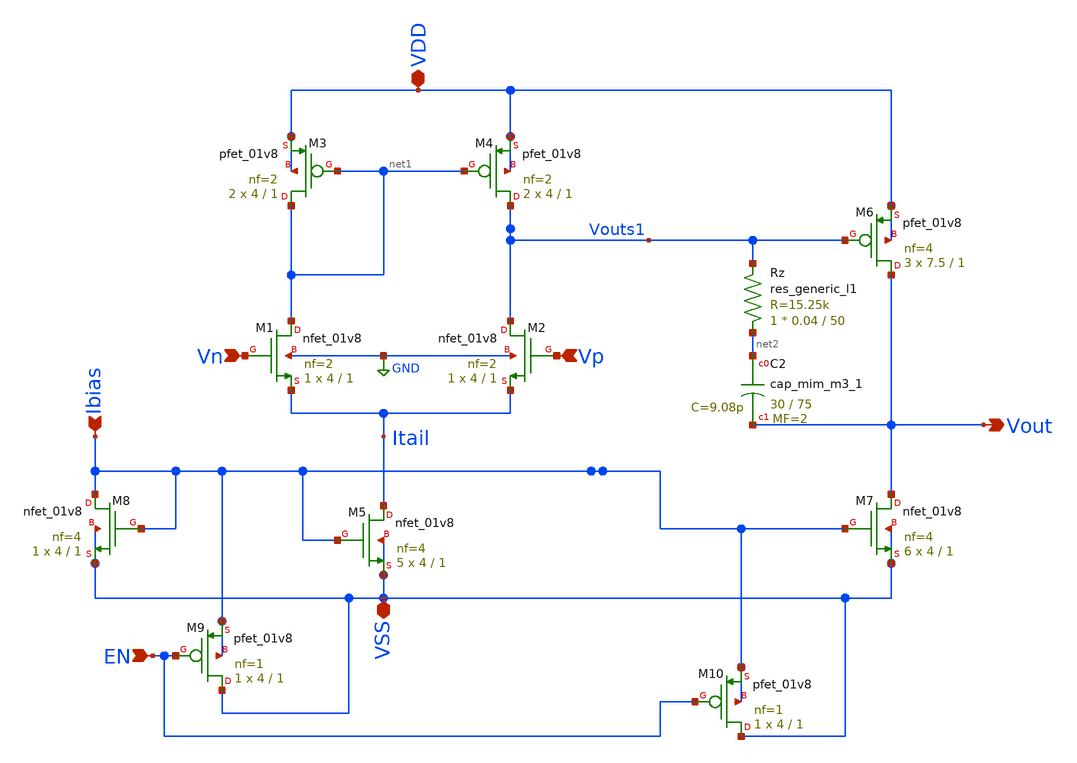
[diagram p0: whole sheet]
** sch_path: xschem/Opamp.sch
**.subckt Opamp Vn Ibias Vp EN Vout VSS VDD
*.ipin Vn
*.ipin Ibias
*.ipin Vp
*.ipin EN
*.opin Vout
*.iopin VSS
*.iopin VDD
XM2 Vouts1 Vp Itail GND sky130_fd_pr__nfet_01v8 L=1 W=4 nf=2 ad='int((nf+1)/2) * W/nf * 0.29' as='int((nf+2)/2) * W/nf * 0.29'
+ pd='2*int((nf+1)/2) * (W/nf + 0.29)' ps='2*int((nf+2)/2) * (W/nf + 0.29)' nrd='0.29 / W' nrs='0.29 / W'
+ sa=0 sb=0 sd=0 mult=1 m=1
XM4 Vouts1 net1 VDD VDD sky130_fd_pr__pfet_01v8 L=1 W=4 nf=2 ad='int((nf+1)/2) * W/nf * 0.29' as='int((nf+2)/2) * W/nf * 0.29'
+ pd='2*int((nf+1)/2) * (W/nf + 0.29)' ps='2*int((nf+2)/2) * (W/nf + 0.29)' nrd='0.29 / W' nrs='0.29 / W'
+ sa=0 sb=0 sd=0 mult=2 m=2
XM3 net1 net1 VDD VDD sky130_fd_pr__pfet_01v8 L=1 W=4 nf=2 ad='int((nf+1)/2) * W/nf * 0.29' as='int((nf+2)/2) * W/nf * 0.29'
+ pd='2*int((nf+1)/2) * (W/nf + 0.29)' ps='2*int((nf+2)/2) * (W/nf + 0.29)' nrd='0.29 / W' nrs='0.29 / W'
+ sa=0 sb=0 sd=0 mult=2 m=2
XM1 net1 Vn Itail GND sky130_fd_pr__nfet_01v8 L=1 W=4 nf=2 ad='int((nf+1)/2) * W/nf * 0.29' as='int((nf+2)/2) * W/nf * 0.29'
+ pd='2*int((nf+1)/2) * (W/nf + 0.29)' ps='2*int((nf+2)/2) * (W/nf + 0.29)' nrd='0.29 / W' nrs='0.29 / W'
+ sa=0 sb=0 sd=0 mult=1 m=1
XM6 Vout Vouts1 VDD VDD sky130_fd_pr__pfet_01v8 L=1 W=7.5 nf=4 ad='int((nf+1)/2) * W/nf * 0.29' as='int((nf+2)/2) * W/nf * 0.29'
+ pd='2*int((nf+1)/2) * (W/nf + 0.29)' ps='2*int((nf+2)/2) * (W/nf + 0.29)' nrd='0.29 / W' nrs='0.29 / W'
+ sa=0 sb=0 sd=0 mult=3 m=3
XM5 Itail Ibias VSS VSS sky130_fd_pr__nfet_01v8 L=1 W=4 nf=4 ad='int((nf+1)/2) * W/nf * 0.29' as='int((nf+2)/2) * W/nf * 0.29'
+ pd='2*int((nf+1)/2) * (W/nf + 0.29)' ps='2*int((nf+2)/2) * (W/nf + 0.29)' nrd='0.29 / W' nrs='0.29 / W'
+ sa=0 sb=0 sd=0 mult=5 m=5
XM7 Vout Ibias VSS VSS sky130_fd_pr__nfet_01v8 L=1 W=4 nf=4 ad='int((nf+1)/2) * W/nf * 0.29' as='int((nf+2)/2) * W/nf * 0.29'
+ pd='2*int((nf+1)/2) * (W/nf + 0.29)' ps='2*int((nf+2)/2) * (W/nf + 0.29)' nrd='0.29 / W' nrs='0.29 / W'
+ sa=0 sb=0 sd=0 mult=6 m=6
XM8 Ibias Ibias VSS VSS sky130_fd_pr__nfet_01v8 L=1 W=4 nf=4 ad='int((nf+1)/2) * W/nf * 0.29' as='int((nf+2)/2) * W/nf * 0.29'
+ pd='2*int((nf+1)/2) * (W/nf + 0.29)' ps='2*int((nf+2)/2) * (W/nf + 0.29)' nrd='0.29 / W' nrs='0.29 / W'
+ sa=0 sb=0 sd=0 mult=1 m=1
XM9 VSS EN Ibias Ibias sky130_fd_pr__pfet_01v8 L=1 W=4 nf=1 ad='int((nf+1)/2) * W/nf * 0.29' as='int((nf+2)/2) * W/nf * 0.29'
+ pd='2*int((nf+1)/2) * (W/nf + 0.29)' ps='2*int((nf+2)/2) * (W/nf + 0.29)' nrd='0.29 / W' nrs='0.29 / W'
+ sa=0 sb=0 sd=0 mult=1 m=1
XM10 VSS EN Ibias Ibias sky130_fd_pr__pfet_01v8 L=1 W=4 nf=1 ad='int((nf+1)/2) * W/nf * 0.29' as='int((nf+2)/2) * W/nf * 0.29'
+ pd='2*int((nf+1)/2) * (W/nf + 0.29)' ps='2*int((nf+2)/2) * (W/nf + 0.29)' nrd='0.29 / W' nrs='0.29 / W'
+ sa=0 sb=0 sd=0 mult=1 m=1
XC2 net2 Vout sky130_fd_pr__cap_mim_m3_1 W=30 L=75 MF=2 m=2
Rz net2 Vouts1 sky130_fd_pr__res_generic_l1 W=0.04 L=50 m=1
**** begin user architecture code

** opencircuitdesign pdks install
.lib /foss/pdks/sky130A/libs.tech/ngspice/sky130.lib.spice tt


"Is Subcircuit" = YES
**** end user architecture code
**.ends
.GLOBAL GND
.end
